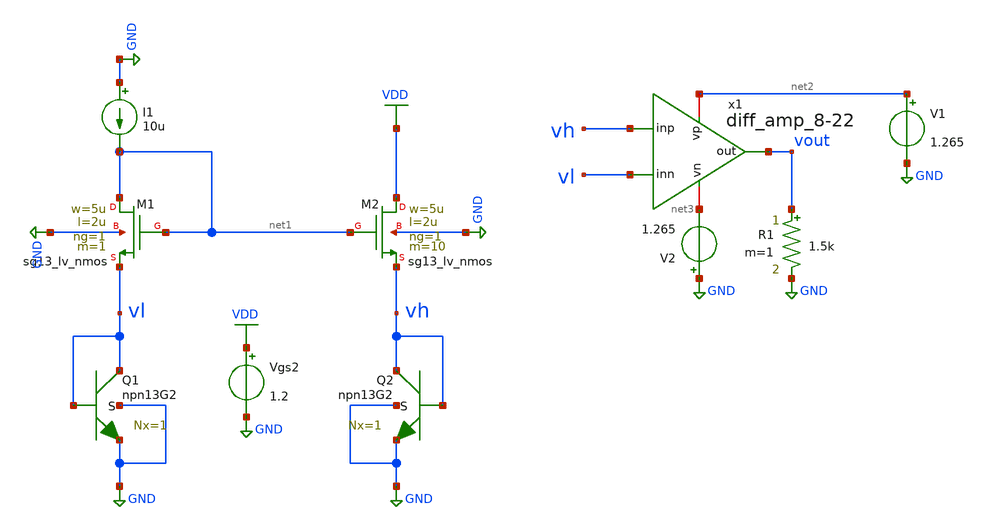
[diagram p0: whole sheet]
** sch_path: TempSensor/design_data/xschem/ptat_bjt_nmos_curr-mirror_amp_tb.sch
**.subckt ptat_bjt_nmos_curr-mirror_amp_tb
XM1 net1 net1 vl GND sg13_lv_nmos w=5u l=2u ng=1 m=1 mm_ok=1
XM2 VDD net1 vh GND sg13_lv_nmos w=5u l=2u ng=1 m=10 mm_ok=1
I1 GND net1 10u
Vgs2 VDD GND 1.2
XQ1 vl vl GND GND npn13G2 Nx=1 mm_ok=1
XQ2 vh vh GND GND npn13G2 Nx=1 mm_ok=1
V1 net2 GND 1.265
V2 GND net3 1.265
x1 net2 vout vh vl net3 diff_amp_8-22
R1 vout GND 1.5k m=1
**** begin user architecture code


.control

save all
dc temp 0 125 1
let indiff = vh - vl

write ptat_bjt_nmos_curr-mirror_amp_tb.raw vout indiff
.endc




** IHP models
.lib cornerMOSlv.lib mos_tt
.lib cornerCAP.lib cap_typ
.lib cornerRES.lib res_typ
.lib cornerHBT.lib hbt_typ


**** end user architecture code
**.ends

* expanding   symbol:  practicing/TempSensor/design_data/xschem/diff_amp_8-22.sym # of pins=5
** sym_path: TempSensor/design_data/xschem/diff_amp_8-22.sym
** sch_path: TempSensor/design_data/xschem/diff_amp_8-22.sch
.subckt diff_amp_8-22 vp out inp inn vn
*.opin out
*.iopin vn
*.iopin vp
*.ipin inp
*.ipin inn
XM5 net18 net1 vp vp sg13_lv_pmos w=10u l=3.33u ng=1 m=1 mm_ok=1
XM30 net15 inn net6 vn sg13_lv_nmos w=10u l=1.5u ng=1 m=5 mm_ok=1
I0 vp net4 5u
XM7 net19 net1 vp vp sg13_lv_pmos w=10u l=3.33u ng=1 m=2 mm_ok=1
XM6 net1 net1 net18 vp sg13_lv_pmos w=10u l=1u ng=1 m=1 mm_ok=1
XM8 net5 net1 net19 vp sg13_lv_pmos w=10u l=.5u ng=1 m=1 mm_ok=1
XM11 net15 net7 vp vp sg13_lv_pmos w=10u l=2.5u ng=1 m=5 mm_ok=1
XM13 net16 net7 vp vp sg13_lv_pmos w=10u l=2.5u ng=1 m=5 mm_ok=1
XM12 net7 net7 net15 vp sg13_lv_pmos w=10u l=1u ng=1 m=5 mm_ok=1
XM14 out net7 net16 vp sg13_lv_pmos w=10u l=1u ng=1 m=5 mm_ok=1
XM21 net12 net12 vp vp sg13_lv_pmos w=10u l=.33u ng=1 m=10 mm_ok=1
XM24 net13 net1 vp vp sg13_lv_pmos w=4u l=5u ng=1 m=1 mm_ok=1
XM22 net11 net11 net12 vp sg13_lv_pmos w=10u l=.33u ng=1 m=10 mm_ok=1
XM29 vp inp net6 vn sg13_lv_nmos w=10u l=1.5u ng=1 m=5 mm_ok=1
XM9 net9 inp net5 net5 sg13_lv_pmos w=10u l=1.5u ng=1 m=10 mm_ok=1
XM10 net8 inn net5 net5 sg13_lv_pmos w=10u l=1.5u ng=1 m=10 mm_ok=1
XM1 net4 net4 net3 vn sg13_lv_nmos w=10u l=2u ng=1 m=1 mm_ok=1
XM2 net3 net4 vn vn sg13_lv_nmos w=5u l=5u ng=1 m=1 mm_ok=1
XM3 net1 net4 net2 vn sg13_lv_nmos w=10u l=2u ng=1 m=1 mm_ok=1
XM4 net2 net4 vn vn sg13_lv_nmos w=5u l=5u ng=1 m=1 mm_ok=1
XM31 net6 net4 net17 vn sg13_lv_nmos w=10u l=1u ng=1 m=1 mm_ok=1
XM32 net17 net4 vn vn sg13_lv_nmos w=10u l=5u ng=1 m=1 mm_ok=1
XM15 net7 net4 net8 vn sg13_lv_nmos w=10u l=1u ng=1 m=5 mm_ok=1
XM16 net8 net4 vn vn sg13_lv_nmos w=10u l=5u ng=1 m=1 mm_ok=1
XM17 net10 net4 net9 vn sg13_lv_nmos w=10u l=1u ng=1 m=5 mm_ok=1
XM18 net9 net4 vn vn sg13_lv_nmos w=10u l=5u ng=1 m=1 mm_ok=1
XM20 net11 net4 vn vn sg13_lv_nmos w=1.5u l=5u ng=1 m=1 mm_ok=1
XM19 net10 net11 out vp sg13_lv_pmos w=10u l=.33u ng=1 m=10 mm_ok=1
XM23 out net13 net10 vn sg13_lv_nmos w=10u l=.5u ng=1 m=5 mm_ok=1
XM25 net13 net13 net14 vn sg13_lv_nmos w=10u l=.5u ng=1 m=5 mm_ok=1
XM26 net14 net14 vn vn sg13_lv_nmos w=10u l=.5u ng=1 m=5 mm_ok=1
XM27 vp out out vp sg13_lv_nmos w=10u l=.33u ng=1 m=10 mm_ok=1
XM28 vn net10 out vn sg13_lv_pmos w=10u l=.5u ng=1 m=5 mm_ok=1
XC1 out out cap_cmim w=3.5e-5 l=3.5e-5 m=1 mm_ok=1
XC2 out net10 cap_cmim w=3.5e-5 l=3.5e-5 m=1 mm_ok=1
.ends

.GLOBAL GND
.GLOBAL VDD
.end
